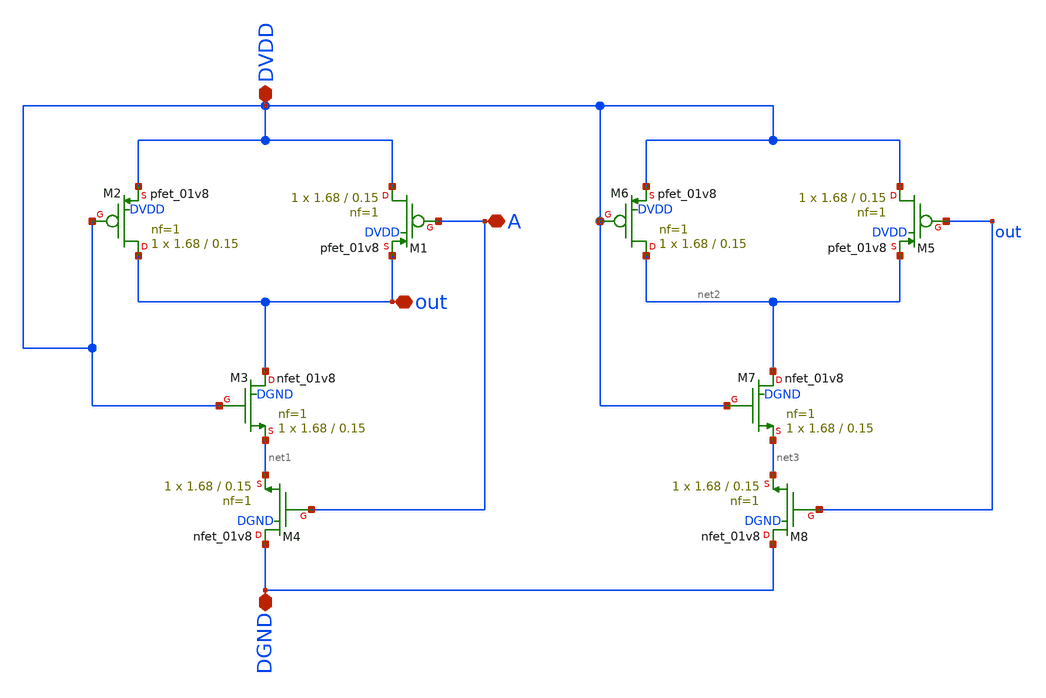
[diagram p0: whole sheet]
** sch_path: tutorial-5/source/nand2.sch
**.subckt nand2 DVDD DGND A out
*.iopin DVDD
*.iopin DGND
*.iopin A
*.iopin out
XM1 DVDD A out DVDD sky130_fd_pr__pfet_01v8 L=0.15 W=1.68 nf=1 ad='int((nf+1)/2) * W/nf * 0.29' as='int((nf+2)/2) * W/nf * 0.29'
+ pd='2*int((nf+1)/2) * (W/nf + 0.29)' ps='2*int((nf+2)/2) * (W/nf + 0.29)' nrd='0.29 / W' nrs='0.29 / W'
+ sa=0 sb=0 sd=0 mult=1 m=1
XM2 out DVDD DVDD DVDD sky130_fd_pr__pfet_01v8 L=0.15 W=1.68 nf=1 ad='int((nf+1)/2) * W/nf * 0.29' as='int((nf+2)/2) * W/nf * 0.29'
+ pd='2*int((nf+1)/2) * (W/nf + 0.29)' ps='2*int((nf+2)/2) * (W/nf + 0.29)' nrd='0.29 / W' nrs='0.29 / W'
+ sa=0 sb=0 sd=0 mult=1 m=1
XM3 out DVDD net1 DGND sky130_fd_pr__nfet_01v8 L=0.15 W=1.68 nf=1 ad='int((nf+1)/2) * W/nf * 0.29' as='int((nf+2)/2) * W/nf * 0.29'
+ pd='2*int((nf+1)/2) * (W/nf + 0.29)' ps='2*int((nf+2)/2) * (W/nf + 0.29)' nrd='0.29 / W' nrs='0.29 / W'
+ sa=0 sb=0 sd=0 mult=1 m=1
XM4 DGND A net1 DGND sky130_fd_pr__nfet_01v8 L=0.15 W=1.68 nf=1 ad='int((nf+1)/2) * W/nf * 0.29' as='int((nf+2)/2) * W/nf * 0.29'
+ pd='2*int((nf+1)/2) * (W/nf + 0.29)' ps='2*int((nf+2)/2) * (W/nf + 0.29)' nrd='0.29 / W' nrs='0.29 / W'
+ sa=0 sb=0 sd=0 mult=1 m=1
XM5 DVDD out net2 DVDD sky130_fd_pr__pfet_01v8 L=0.15 W=1.68 nf=1 ad='int((nf+1)/2) * W/nf * 0.29' as='int((nf+2)/2) * W/nf * 0.29'
+ pd='2*int((nf+1)/2) * (W/nf + 0.29)' ps='2*int((nf+2)/2) * (W/nf + 0.29)' nrd='0.29 / W' nrs='0.29 / W'
+ sa=0 sb=0 sd=0 mult=1 m=1
XM6 net2 DVDD DVDD DVDD sky130_fd_pr__pfet_01v8 L=0.15 W=1.68 nf=1 ad='int((nf+1)/2) * W/nf * 0.29' as='int((nf+2)/2) * W/nf * 0.29'
+ pd='2*int((nf+1)/2) * (W/nf + 0.29)' ps='2*int((nf+2)/2) * (W/nf + 0.29)' nrd='0.29 / W' nrs='0.29 / W'
+ sa=0 sb=0 sd=0 mult=1 m=1
XM7 net2 DVDD net3 DGND sky130_fd_pr__nfet_01v8 L=0.15 W=1.68 nf=1 ad='int((nf+1)/2) * W/nf * 0.29' as='int((nf+2)/2) * W/nf * 0.29'
+ pd='2*int((nf+1)/2) * (W/nf + 0.29)' ps='2*int((nf+2)/2) * (W/nf + 0.29)' nrd='0.29 / W' nrs='0.29 / W'
+ sa=0 sb=0 sd=0 mult=1 m=1
XM8 DGND out net3 DGND sky130_fd_pr__nfet_01v8 L=0.15 W=1.68 nf=1 ad='int((nf+1)/2) * W/nf * 0.29' as='int((nf+2)/2) * W/nf * 0.29'
+ pd='2*int((nf+1)/2) * (W/nf + 0.29)' ps='2*int((nf+2)/2) * (W/nf + 0.29)' nrd='0.29 / W' nrs='0.29 / W'
+ sa=0 sb=0 sd=0 mult=1 m=1
**.ends
.end
